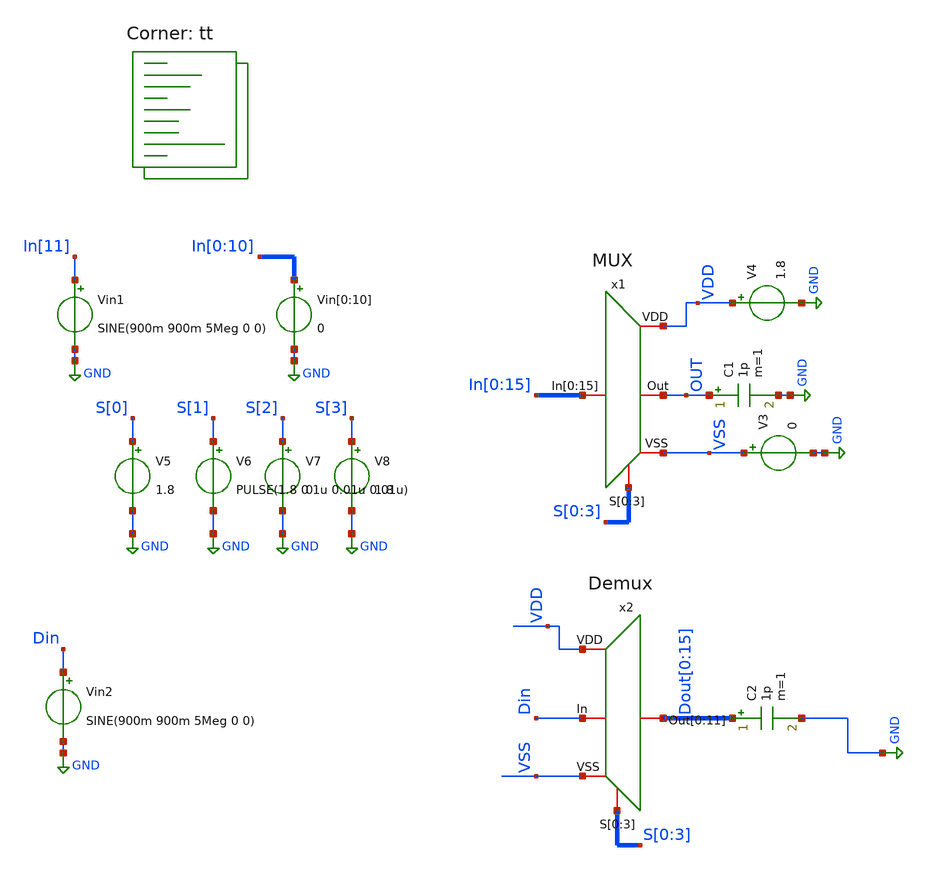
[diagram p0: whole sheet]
** sch_path: MUX/TB_MUX.sch
**.subckt TB_MUX
x1 VDD VSS In[0] In[1] In[2] In[3] In[4] In[5] In[6] In[7] In[8] In[9] In[10] In[11] In[12] In[13]
+ In[14] In[15] OUT S[0] S[1] S[2] S[3] MUX
Vin1 In[11] GND SINE(900m 900m 5Meg 0 0)
V4 VDD GND 1.8
V5 S[0] GND 1.8
V6 S[1] GND PULSE(1.8 0 1u 0.01u 0.01u)
V7 S[2] GND 0
V8 S[3] GND 1.8
V3 VSS GND 0
C1 OUT GND 1p m=1
Vin[0] In[0] GND 0
Vin[1] In[1] GND 0
Vin[2] In[2] GND 0
Vin[3] In[3] GND 0
Vin[4] In[4] GND 0
Vin[5] In[5] GND 0
Vin[6] In[6] GND 0
Vin[7] In[7] GND 0
Vin[8] In[8] GND 0
Vin[9] In[9] GND 0
Vin[10] In[10] GND 0
Vin2 Din GND SINE(900m 900m 5Meg 0 0)
C2 Dout[0] GND 1p m=1
x2 Dout[0] Dout[1] Dout[2] Dout[3] Dout[4] Dout[5] Dout[6] Dout[7] Dout[8] Dout[9] Dout[10] Dout[11]
+ Din VDD VSS S[0] S[1] S[2] S[3] Demux
**** begin user architecture code


.tran 0.001u 2u
.save all


.lib $::SKYWATER_MODELS/sky130.lib.spice tt
**** end user architecture code
**.ends

* expanding   symbol:  MUX.sym # of pins=5
** sym_path: MUX/MUX.sym
** sch_path: MUX/MUX.sch
.subckt MUX VDD VSS In[0] In[1] In[2] In[3] In[4] In[5] In[6] In[7] In[8] In[9] In[10] In[11] In[12]
+ In[13] In[14] In[15] Out S[0] S[1] S[2] S[3]
*.iopin VDD
*.iopin VSS
*.iopin
*+ In[0],In[1],In[2],In[3],In[4],In[5],In[6],In[7],In[8],In[9],In[10],In[11],In[12],In[13],In[14],In[15]
*.iopin Out
*.iopin S[0],S[1],S[2],S[3]
X[0] S[0] VDD R0[0] In[0] VSS S[0]B MUX_TG
x1 VDD S[0]B S[0] VSS inverter
X[13] S[1] VDD R1[0] R0[0] VSS S[1]B MUX_TG
x2 VDD S[1]B S[1] VSS inverter
X[19] S[2] VDD R2[0] R1[0] VSS S[2]B MUX_TG
x3 VDD S[2]B S[2] VSS inverter
x4 VDD S[3]B S[3] VSS inverter
X[22] S[3] VDD Out R2[0] VSS S[3]B MUX_TG
X[1] S[0]B VDD R0[0] In[1] VSS S[0] MUX_TG
X[14] S[1]B VDD R1[0] R0[1] VSS S[1] MUX_TG
X[20] S[2]B VDD R2[0] R1[1] VSS S[2] MUX_TG
X[23] S[3]B VDD Out R2[1] VSS S[3] MUX_TG
X[2] S[0] VDD R0[1] In[2] VSS S[0]B MUX_TG
X[15] S[1] VDD R1[1] R0[2] VSS S[1]B MUX_TG
X[21] S[2] VDD R2[1] R1[2] VSS S[2]B MUX_TG
X[3] S[0]B VDD R0[1] In[3] VSS S[0] MUX_TG
X[16] S[1]B VDD R1[1] R0[3] VSS S[1] MUX_TG
X[4] S[0] VDD R0[2] In[4] VSS S[0]B MUX_TG
X[17] S[1] VDD R1[2] R0[4] VSS S[1]B MUX_TG
X[5] S[0]B VDD R0[2] In[5] VSS S[0] MUX_TG
X[18] S[1]B VDD R1[2] R0[5] VSS S[1] MUX_TG
X[6] S[0] VDD R0[3] In[6] VSS S[0]B MUX_TG
X[7] S[0]B VDD R0[3] In[7] VSS S[0] MUX_TG
X[8] S[0] VDD R0[4] In[8] VSS S[0]B MUX_TG
X[9] S[0]B VDD R0[4] In[9] VSS S[0] MUX_TG
X[10] S[0] VDD R0[5] In[10] VSS S[0]B MUX_TG
X[11] S[0]B VDD R0[5] In[11] VSS S[0] MUX_TG
.ends


* expanding   symbol:  Demux.sym # of pins=5
** sym_path: MUX/Demux.sym
** sch_path: MUX/Demux.sch
.subckt Demux Out[0] Out[1] Out[2] Out[3] Out[4] Out[5] Out[6] Out[7] Out[8] Out[9] Out[10] Out[11]
+ In VDD VSS S[0] S[1] S[2] S[3]
*.iopin S[0],S[1],S[2],S[3]
*.iopin VSS
*.iopin VDD
*.iopin Out[0],Out[1],Out[2],Out[3],Out[4],Out[5],Out[6],Out[7],Out[8],Out[9],Out[10],Out[11]
*.iopin In
x5 VDD In S[0]B S[1]B S[2]B S[3]B Out[0] VSS AND
x6 VDD In S[0] S[1]B S[2]B S[3]B Out[1] VSS AND
x7 VDD In S[0]B S[1] S[2]B S[3]B Out[2] VSS AND
x8 VDD In S[0] S[1] S[2]B S[3]B Out[3] VSS AND
x9 VDD In S[0]B S[1]B S[2] S[3]B Out[4] VSS AND
x10 VDD In S[0] S[1]B S[2] S[3]B Out[5] VSS AND
x11 VDD In S[0]B S[1] S[2] S[3]B Out[6] VSS AND
x12 VDD In S[0] S[1] S[2] S[3]B Out[7] VSS AND
x13 VDD In S[0]B S[1]B S[2]B S[3] Out[8] VSS AND
x14 VDD In S[0] S[1]B S[2]B S[3] Out[9] VSS AND
x15 VDD In S[0]B S[1] S[2]B S[3] Out[10] VSS AND
x16 VDD In S[0] S[1] S[2]B S[3] Out[11] VSS AND
x1 VDD S[0]B S[0] VSS inverter_demux
x2 VDD S[1]B S[1] VSS inverter_demux
x3 VDD S[2]B S[2] VSS inverter_demux
x4 VDD S[3]B S[3] VSS inverter_demux
.ends


* expanding   symbol:  MUX_TG.sym # of pins=6
** sym_path: MUX/MUX_TG.sym
** sch_path: MUX/MUX_TG.sch
.subckt MUX_TG AB VDD Out In VSS A
*.iopin In
*.iopin Out
*.iopin VDD
*.iopin VSS
*.iopin AB
*.iopin A
XM1 In A Out VSS sky130_fd_pr__nfet_01v8 L=0.15 W=2.1 nf=1 ad='int((nf+1)/2) * W/nf * 0.29' as='int((nf+2)/2) * W/nf * 0.29'
+ pd='2*int((nf+1)/2) * (W/nf + 0.29)' ps='2*int((nf+2)/2) * (W/nf + 0.29)' nrd='0.29 / W' nrs='0.29 / W'
+ sa=0 sb=0 sd=0 mult=2 m=2
XM2 In AB Out VDD sky130_fd_pr__pfet_01v8 L=0.15 W=4.75 nf=1 ad='int((nf+1)/2) * W/nf * 0.29' as='int((nf+2)/2) * W/nf * 0.29'
+ pd='2*int((nf+1)/2) * (W/nf + 0.29)' ps='2*int((nf+2)/2) * (W/nf + 0.29)' nrd='0.29 / W' nrs='0.29 / W'
+ sa=0 sb=0 sd=0 mult=4 m=4
.ends


* expanding   symbol:  inverter.sym # of pins=4
** sym_path: MUX/inverter.sym
** sch_path: MUX/inverter.sch
.subckt inverter VDD Out In VSS
*.iopin VDD
*.iopin Out
*.iopin VSS
*.iopin In
XM3 Out In VSS VSS sky130_fd_pr__nfet_01v8 L=0.15 W=2.1 nf=1 ad='int((nf+1)/2) * W/nf * 0.29' as='int((nf+2)/2) * W/nf * 0.29'
+ pd='2*int((nf+1)/2) * (W/nf + 0.29)' ps='2*int((nf+2)/2) * (W/nf + 0.29)' nrd='0.29 / W' nrs='0.29 / W'
+ sa=0 sb=0 sd=0 mult=2 m=2
XM1 Out In VDD VDD sky130_fd_pr__pfet_01v8 L=0.15 W=4.75 nf=1 ad='int((nf+1)/2) * W/nf * 0.29' as='int((nf+2)/2) * W/nf * 0.29'
+ pd='2*int((nf+1)/2) * (W/nf + 0.29)' ps='2*int((nf+2)/2) * (W/nf + 0.29)' nrd='0.29 / W' nrs='0.29 / W'
+ sa=0 sb=0 sd=0 mult=4 m=4
.ends


* expanding   symbol:  AND.sym # of pins=8
** sym_path: MUX/AND.sym
** sch_path: MUX/AND.sch
.subckt AND VDD E A B C D Out VSS
*.iopin VDD
*.iopin A
*.iopin VSS
*.iopin B
*.iopin Out
*.iopin C
*.iopin D
*.iopin E
XM3 net1 A net2 VSS sky130_fd_pr__nfet_01v8 L=0.15 W=0.65 nf=1 ad='int((nf+1)/2) * W/nf * 0.29' as='int((nf+2)/2) * W/nf * 0.29'
+ pd='2*int((nf+1)/2) * (W/nf + 0.29)' ps='2*int((nf+2)/2) * (W/nf + 0.29)' nrd='0.29 / W' nrs='0.29 / W'
+ sa=0 sb=0 sd=0 mult=1 m=1
XM1 net1 A VDD VDD sky130_fd_pr__pfet_01v8 L=0.15 W=1 nf=1 ad='int((nf+1)/2) * W/nf * 0.29' as='int((nf+2)/2) * W/nf * 0.29'
+ pd='2*int((nf+1)/2) * (W/nf + 0.29)' ps='2*int((nf+2)/2) * (W/nf + 0.29)' nrd='0.29 / W' nrs='0.29 / W'
+ sa=0 sb=0 sd=0 mult=1 m=1
XM5 Out net1 VSS VSS sky130_fd_pr__nfet_01v8 L=0.15 W=0.65 nf=1 ad='int((nf+1)/2) * W/nf * 0.29' as='int((nf+2)/2) * W/nf * 0.29'
+ pd='2*int((nf+1)/2) * (W/nf + 0.29)' ps='2*int((nf+2)/2) * (W/nf + 0.29)' nrd='0.29 / W' nrs='0.29 / W'
+ sa=0 sb=0 sd=0 mult=1 m=1
XM6 Out net1 VDD VDD sky130_fd_pr__pfet_01v8 L=0.15 W=1 nf=1 ad='int((nf+1)/2) * W/nf * 0.29' as='int((nf+2)/2) * W/nf * 0.29'
+ pd='2*int((nf+1)/2) * (W/nf + 0.29)' ps='2*int((nf+2)/2) * (W/nf + 0.29)' nrd='0.29 / W' nrs='0.29 / W'
+ sa=0 sb=0 sd=0 mult=1 m=1
XM4 net1 B VDD VDD sky130_fd_pr__pfet_01v8 L=0.15 W=1 nf=1 ad='int((nf+1)/2) * W/nf * 0.29' as='int((nf+2)/2) * W/nf * 0.29'
+ pd='2*int((nf+1)/2) * (W/nf + 0.29)' ps='2*int((nf+2)/2) * (W/nf + 0.29)' nrd='0.29 / W' nrs='0.29 / W'
+ sa=0 sb=0 sd=0 mult=1 m=1
XM10 net1 C VDD VDD sky130_fd_pr__pfet_01v8 L=0.15 W=1 nf=1 ad='int((nf+1)/2) * W/nf * 0.29' as='int((nf+2)/2) * W/nf * 0.29'
+ pd='2*int((nf+1)/2) * (W/nf + 0.29)' ps='2*int((nf+2)/2) * (W/nf + 0.29)' nrd='0.29 / W' nrs='0.29 / W'
+ sa=0 sb=0 sd=0 mult=1 m=1
XM11 net1 D VDD VDD sky130_fd_pr__pfet_01v8 L=0.15 W=1 nf=1 ad='int((nf+1)/2) * W/nf * 0.29' as='int((nf+2)/2) * W/nf * 0.29'
+ pd='2*int((nf+1)/2) * (W/nf + 0.29)' ps='2*int((nf+2)/2) * (W/nf + 0.29)' nrd='0.29 / W' nrs='0.29 / W'
+ sa=0 sb=0 sd=0 mult=1 m=1
XM12 net1 E VDD VDD sky130_fd_pr__pfet_01v8 L=0.15 W=1 nf=1 ad='int((nf+1)/2) * W/nf * 0.29' as='int((nf+2)/2) * W/nf * 0.29'
+ pd='2*int((nf+1)/2) * (W/nf + 0.29)' ps='2*int((nf+2)/2) * (W/nf + 0.29)' nrd='0.29 / W' nrs='0.29 / W'
+ sa=0 sb=0 sd=0 mult=1 m=1
XM2 net2 B net5 VSS sky130_fd_pr__nfet_01v8 L=0.15 W=0.65 nf=1 ad='int((nf+1)/2) * W/nf * 0.29' as='int((nf+2)/2) * W/nf * 0.29'
+ pd='2*int((nf+1)/2) * (W/nf + 0.29)' ps='2*int((nf+2)/2) * (W/nf + 0.29)' nrd='0.29 / W' nrs='0.29 / W'
+ sa=0 sb=0 sd=0 mult=1 m=1
XM7 net5 C net4 VSS sky130_fd_pr__nfet_01v8 L=0.15 W=0.65 nf=1 ad='int((nf+1)/2) * W/nf * 0.29' as='int((nf+2)/2) * W/nf * 0.29'
+ pd='2*int((nf+1)/2) * (W/nf + 0.29)' ps='2*int((nf+2)/2) * (W/nf + 0.29)' nrd='0.29 / W' nrs='0.29 / W'
+ sa=0 sb=0 sd=0 mult=1 m=1
XM8 net4 D net3 VSS sky130_fd_pr__nfet_01v8 L=0.15 W=0.65 nf=1 ad='int((nf+1)/2) * W/nf * 0.29' as='int((nf+2)/2) * W/nf * 0.29'
+ pd='2*int((nf+1)/2) * (W/nf + 0.29)' ps='2*int((nf+2)/2) * (W/nf + 0.29)' nrd='0.29 / W' nrs='0.29 / W'
+ sa=0 sb=0 sd=0 mult=1 m=1
XM9 net3 E VSS VSS sky130_fd_pr__nfet_01v8 L=0.15 W=0.65 nf=1 ad='int((nf+1)/2) * W/nf * 0.29' as='int((nf+2)/2) * W/nf * 0.29'
+ pd='2*int((nf+1)/2) * (W/nf + 0.29)' ps='2*int((nf+2)/2) * (W/nf + 0.29)' nrd='0.29 / W' nrs='0.29 / W'
+ sa=0 sb=0 sd=0 mult=1 m=1
.ends


* expanding   symbol:  inverter_demux.sym # of pins=4
** sym_path: MUX/inverter_demux.sym
** sch_path: MUX/inverter_demux.sch
.subckt inverter_demux VDD Out In VSS
*.iopin VDD
*.iopin Out
*.iopin VSS
*.iopin In
XM3 Out In VSS VSS sky130_fd_pr__nfet_01v8 L=0.15 W=0.65 nf=1 ad='int((nf+1)/2) * W/nf * 0.29' as='int((nf+2)/2) * W/nf * 0.29'
+ pd='2*int((nf+1)/2) * (W/nf + 0.29)' ps='2*int((nf+2)/2) * (W/nf + 0.29)' nrd='0.29 / W' nrs='0.29 / W'
+ sa=0 sb=0 sd=0 mult=1 m=1
XM1 Out In VDD VDD sky130_fd_pr__pfet_01v8 L=0.15 W=1 nf=1 ad='int((nf+1)/2) * W/nf * 0.29' as='int((nf+2)/2) * W/nf * 0.29'
+ pd='2*int((nf+1)/2) * (W/nf + 0.29)' ps='2*int((nf+2)/2) * (W/nf + 0.29)' nrd='0.29 / W' nrs='0.29 / W'
+ sa=0 sb=0 sd=0 mult=1 m=1
.ends

.GLOBAL GND
.end
